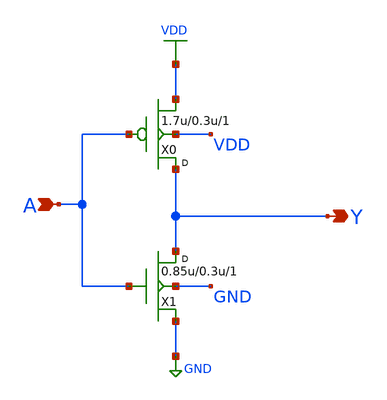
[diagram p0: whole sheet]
** sch_path: openfasoc/common/platforms/gf180mcuosu9Tinv1/gf180mcu_osu_sc_inv_1.sch
**.subckt gf180mcu_osu_sc_inv_1 A Y
*.ipin A
*.opin Y
X0 Y A VDD VDD pmos_3p3 w=1.7u l=0.3u m=1
X1 Y A GND GND nmos_3p3 w=0.85u l=0.3u m=1
**.ends
.GLOBAL VDD
.GLOBAL GND
.end
